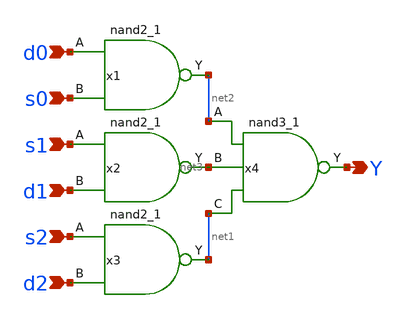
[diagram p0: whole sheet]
** sch_path: elements/logic/mux3.sch
**.subckt mux3 s0 d0 s1 d1 s2 d2 Y
*.ipin s0
*.ipin d0
*.ipin s1
*.ipin d1
*.ipin s2
*.ipin d2
*.opin Y
x1 d0 s0 VSS VSS VCC VCC net2 sky130_fd_sc_hd__nand2_1
x2 s1 d1 VSS VSS VCC VCC net3 sky130_fd_sc_hd__nand2_1
x3 s2 d2 VSS VSS VCC VCC net1 sky130_fd_sc_hd__nand2_1
x4 net2 net3 net1 VSS VSS VCC VCC Y sky130_fd_sc_hd__nand3_1
**.ends
.end
